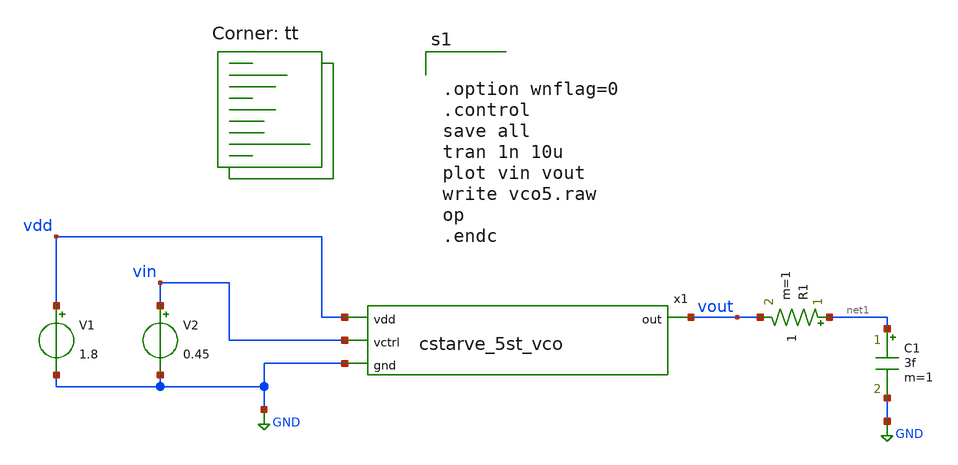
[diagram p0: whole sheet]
** sch_path: xsch/cstarve_5st_vco_tb.sch
**.subckt cstarve_5st_vco_tb
x1 vdd vin vout GND cstarve_5st_vco
V1 vdd GND 1.8
V2 vin GND 0.45
R1 net1 vout 1 m=1
C1 net1 GND 3f m=1
**** begin user architecture code
.lib $::SKYWATER_MODELS/sky130.lib.spice tt


.option wnflag=0
.control
save all
tran 1n 10u
plot vin vout
write vco5.raw
op
.endc


**** end user architecture code
**.ends

* expanding   symbol:  cstarve_5st_vco.sym # of pins=4
** sym_path: xsch/cstarve_5st_vco.sym
** sch_path: xsch/cstarve_5st_vco.sch
.subckt cstarve_5st_vco vdd vctrl out gnd
*.ipin vdd
*.ipin gnd
*.ipin vctrl
*.opin out
x1 vdd net1 net2 out vctrl gnd cstarve_stage
x2 vdd net1 vctrl net6 gnd bias_ctrl
x3 vdd net1 net3 net2 vctrl gnd cstarve_stage
x4 vdd net1 net4 net3 vctrl gnd cstarve_stage
x5 vdd net1 net5 net4 vctrl gnd cstarve_stage
x6 vdd vdd out net5 vctrl gnd cstarve_stage
.ends


* expanding   symbol:  cstarve_stage.sym # of pins=6
** sym_path: xsch/cstarve_stage.sym
** sch_path: xsch/cstarve_stage.sch
.subckt cstarve_stage vdd vcp vout vin vcn gnd
*.ipin vdd
*.ipin gnd
*.ipin vcp
*.ipin vcn
*.ipin vin
*.opin vout
XM1 vout vin net1 gnd sky130_fd_pr__nfet_01v8 L=0.15 W=1 nf=1 ad='int((nf+1)/2) * W/nf * 0.29' as='int((nf+2)/2) * W/nf * 0.29'
+ pd='2*int((nf+1)/2) * (W/nf + 0.29)' ps='2*int((nf+2)/2) * (W/nf + 0.29)' nrd='0.29 / W' nrs='0.29 / W'
+ sa=0 sb=0 sd=0 mult=1 m=1
XM2 vout vin net2 vdd sky130_fd_pr__pfet_01v8 L=0.15 W=2 nf=1 ad='int((nf+1)/2) * W/nf * 0.29' as='int((nf+2)/2) * W/nf * 0.29'
+ pd='2*int((nf+1)/2) * (W/nf + 0.29)' ps='2*int((nf+2)/2) * (W/nf + 0.29)' nrd='0.29 / W' nrs='0.29 / W'
+ sa=0 sb=0 sd=0 mult=1 m=1
XM3 net1 vcn gnd gnd sky130_fd_pr__nfet_01v8 L=0.3 W=1 nf=1 ad='int((nf+1)/2) * W/nf * 0.29' as='int((nf+2)/2) * W/nf * 0.29'
+ pd='2*int((nf+1)/2) * (W/nf + 0.29)' ps='2*int((nf+2)/2) * (W/nf + 0.29)' nrd='0.29 / W' nrs='0.29 / W'
+ sa=0 sb=0 sd=0 mult=1 m=1
XM4 net2 vcp vdd vdd sky130_fd_pr__pfet_01v8 L=0.3 W=2 nf=1 ad='int((nf+1)/2) * W/nf * 0.29' as='int((nf+2)/2) * W/nf * 0.29'
+ pd='2*int((nf+1)/2) * (W/nf + 0.29)' ps='2*int((nf+2)/2) * (W/nf + 0.29)' nrd='0.29 / W' nrs='0.29 / W'
+ sa=0 sb=0 sd=0 mult=1 m=1
.ends


* expanding   symbol:  bias_ctrl.sym # of pins=5
** sym_path: xsch/bias_ctrl.sym
** sch_path: xsch/bias_ctrl.sch
.subckt bias_ctrl vdd vcp vcn source_mn gnd
*.ipin vcn
*.ipin vdd
*.ipin gnd
*.opin vcp
*.opin source_mn
XM2 vcp vcp vdd vdd sky130_fd_pr__pfet_01v8 L=0.3 W=4 nf=1 ad='int((nf+1)/2) * W/nf * 0.29' as='int((nf+2)/2) * W/nf * 0.29'
+ pd='2*int((nf+1)/2) * (W/nf + 0.29)' ps='2*int((nf+2)/2) * (W/nf + 0.29)' nrd='0.29 / W' nrs='0.29 / W'
+ sa=0 sb=0 sd=0 mult=1 m=1
XM1 vcp vcn source_mn gnd sky130_fd_pr__nfet_01v8 L=0.3 W=1 nf=1 ad='int((nf+1)/2) * W/nf * 0.29' as='int((nf+2)/2) * W/nf * 0.29'
+ pd='2*int((nf+1)/2) * (W/nf + 0.29)' ps='2*int((nf+2)/2) * (W/nf + 0.29)' nrd='0.29 / W' nrs='0.29 / W'
+ sa=0 sb=0 sd=0 mult=1 m=1
.ends

.GLOBAL GND
.end
